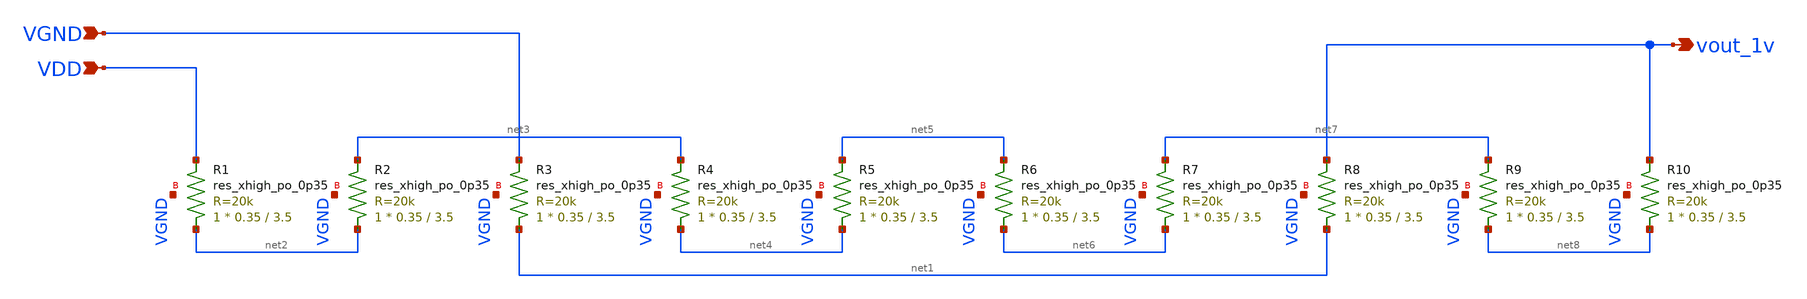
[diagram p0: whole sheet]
** sch_path: xschem/vb_divider.sch
**.subckt vb_divider VDD VGND vout_1v
*.ipin VDD
*.ipin VGND
*.opin vout_1v
XR1 net2 VDD VGND sky130_fd_pr__res_xhigh_po_0p35 L=3.5 mult=1 m=1
XR2 net2 net3 VGND sky130_fd_pr__res_xhigh_po_0p35 L=3.5 mult=1 m=1
XR3 net1 VGND VGND sky130_fd_pr__res_xhigh_po_0p35 L=3.5 mult=1 m=1
XR4 net4 net3 VGND sky130_fd_pr__res_xhigh_po_0p35 L=3.5 mult=1 m=1
XR5 net4 net5 VGND sky130_fd_pr__res_xhigh_po_0p35 L=3.5 mult=1 m=1
XR6 net6 net5 VGND sky130_fd_pr__res_xhigh_po_0p35 L=3.5 mult=1 m=1
XR7 net6 net7 VGND sky130_fd_pr__res_xhigh_po_0p35 L=3.5 mult=1 m=1
XR8 net1 vout_1v VGND sky130_fd_pr__res_xhigh_po_0p35 L=3.5 mult=1 m=1
XR9 net8 net7 VGND sky130_fd_pr__res_xhigh_po_0p35 L=3.5 mult=1 m=1
XR10 net8 vout_1v VGND sky130_fd_pr__res_xhigh_po_0p35 L=3.5 mult=1 m=1
**.ends
.end
